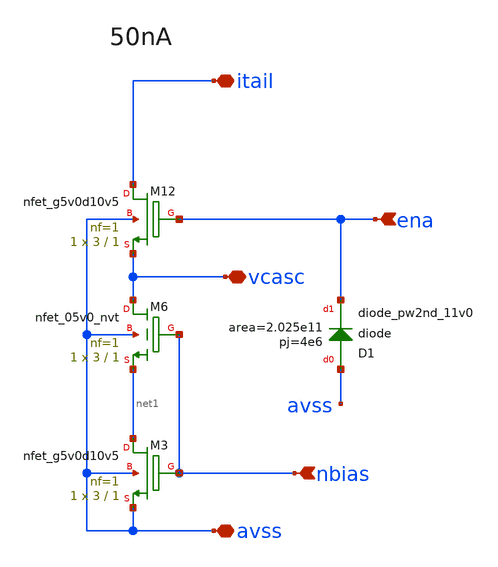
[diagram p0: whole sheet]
** sch_path: xschem/bias_nstack.sch
**.subckt bias_nstack avss ena nbias itail vcasc
*.iopin avss
*.ipin ena
*.ipin nbias
*.iopin itail
*.iopin vcasc
XM3 net1 nbias avss avss sky130_fd_pr__nfet_g5v0d10v5 L=1 W=3 nf=1 ad='int((nf+1)/2) * W/nf * 0.29' as='int((nf+2)/2) * W/nf * 0.29'
+ pd='2*int((nf+1)/2) * (W/nf + 0.29)' ps='2*int((nf+2)/2) * (W/nf + 0.29)' nrd='0.29 / W' nrs='0.29 / W'
+ sa=0 sb=0 sd=0 mult=1 m=1
XM6 vcasc nbias net1 avss sky130_fd_pr__nfet_05v0_nvt L=1 W=3 nf=1 ad='int((nf+1)/2) * W/nf * 0.29' as='int((nf+2)/2) * W/nf * 0.29'
+ pd='2*int((nf+1)/2) * (W/nf + 0.29)' ps='2*int((nf+2)/2) * (W/nf + 0.29)' nrd='0.29 / W' nrs='0.29 / W'
+ sa=0 sb=0 sd=0 mult=1 m=1
XM12 itail ena vcasc avss sky130_fd_pr__nfet_g5v0d10v5 L=1 W=3 nf=1 ad='int((nf+1)/2) * W/nf * 0.29'
+ as='int((nf+2)/2) * W/nf * 0.29' pd='2*int((nf+1)/2) * (W/nf + 0.29)' ps='2*int((nf+2)/2) * (W/nf + 0.29)'
+ nrd='0.29 / W' nrs='0.29 / W' sa=0 sb=0 sd=0 mult=1 m=1
XD1 avss ena sky130_fd_pr__diode_pw2nd_11v0 area=2.025e11 pj=4e6
**.ends
.end
